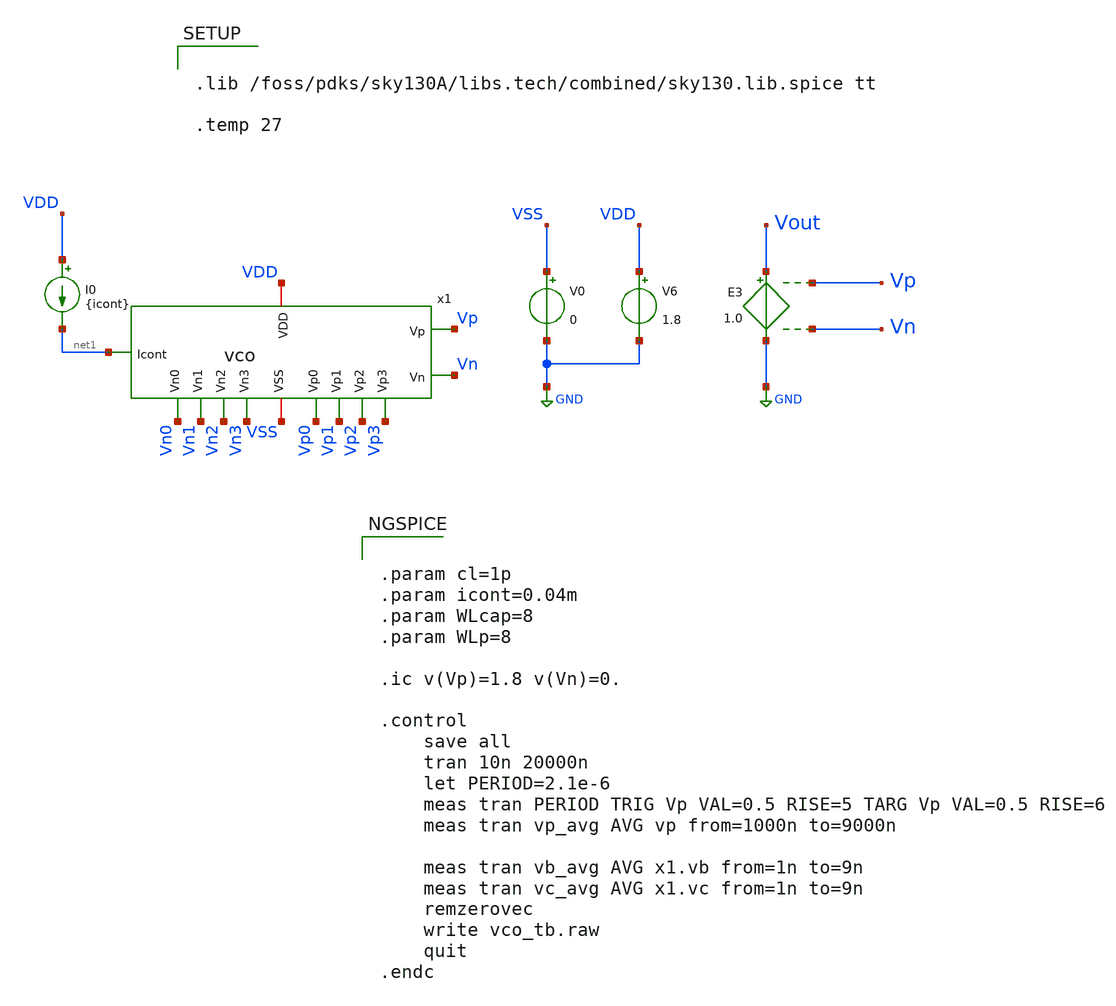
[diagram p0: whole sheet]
** sch_path: xschem/vco_tb.sch
**.subckt vco_tb
V0 VSS GND 0
V6 VDD GND 1.8
I0 VDD net1 {icont}
E3 Vout GND Vp Vn 1.0
x1 VDD VSS net1 Vp Vn Vp0 Vp1 Vp2 Vp3 Vn0 Vn1 Vn2 Vn3 vco
**** begin user architecture code


.param cl=1p
.param icont=0.04m
.param WLcap=8
.param WLp=8

.ic v(Vp)=1.8 v(Vn)=0.

.control
	save all
	tran 10n 20000n
	let PERIOD=2.1e-6
	meas tran PERIOD TRIG Vp VAL=0.5 RISE=5 TARG Vp VAL=0.5 RISE=6
	meas tran vp_avg AVG vp from=1000n to=9000n

	meas tran vb_avg AVG x1.vb from=1n to=9n
	meas tran vc_avg AVG x1.vc from=1n to=9n
	remzerovec
	write vco_tb.raw
	quit
.endc




.lib /foss/pdks/sky130A/libs.tech/combined/sky130.lib.spice tt

.temp 27


**** end user architecture code
**.ends

* expanding   symbol:  vco.sym # of pins=13
** sym_path: xschem/vco.sym
** sch_path: xschem/vco.sch
.subckt vco VDD VSS Icont Vp Vn Vp0 Vp1 Vp2 Vp3 Vn0 Vn1 Vn2 Vn3
*.iopin VDD
*.iopin VSS
*.ipin Icont
*.opin Vp
*.opin Vn
*.opin Vp0
*.opin Vp1
*.opin Vp2
*.opin Vp3
*.opin Vn0
*.opin Vn1
*.opin Vn2
*.opin Vn3
x1 VDD VSS Vp Vn Vb Vc net1 net2 vco_stage
x2 VDD VSS net1 net2 Vb Vc net3 net4 vco_stage
x3 VDD VSS net3 net4 Vb Vc Vpin1 Vnin1 vco_stage
x4 VDD VSS Vpin1 Vnin1 Vb Vc Vn Vp vco_stage
x5 VDD VSS Icont Vb Vc vco_bias
x6 VDD VSS net1 Vp0 vco_buffer
x7 VDD VSS net3 Vp1 vco_buffer
x8 VDD VSS Vpin1 Vp2 vco_buffer
x9 VDD VSS Vn Vp3 vco_buffer
x10 VDD VSS net2 Vn0 vco_buffer
x11 VDD VSS net4 Vn1 vco_buffer
x12 VDD VSS Vnin1 Vn2 vco_buffer
x13 VDD VSS Vp Vn3 vco_buffer
.ends


* expanding   symbol:  vco_stage.sym # of pins=8
** sym_path: xschem/vco_stage.sym
** sch_path: xschem/vco_stage.sch
.subckt vco_stage VDD VSS Vp Vn Vb Vc Vpout Vnout
*.iopin VDD
*.iopin VSS
*.ipin Vp
*.ipin Vn
*.ipin Vb
*.ipin Vc
*.opin Vpout
*.opin Vnout
XM5 Vds_m5 Vc VSS VSS sky130_fd_pr__nfet_01v8 L={L} W={W} nf=2 ad='int((nf+1)/2) * W/nf * 0.29' as='int((nf+2)/2) * W/nf * 0.29'
+ pd='2*int((nf+1)/2) * (W/nf + 0.29)' ps='2*int((nf+2)/2) * (W/nf + 0.29)' nrd='0.29 / W' nrs='0.29 / W'
+ sa=0 sb=0 sd=0 mult=1 m=1
x1 VDD VSS Vp Vb Vnout Vpout Vds_m5 vco_stage_half
x2 VDD VSS Vn Vb Vpout Vnout Vds_m5 vco_stage_half
.ends


* expanding   symbol:  vco_bias.sym # of pins=5
** sym_path: xschem/vco_bias.sym
** sch_path: xschem/vco_bias.sch
.subckt vco_bias VDD VSS Icont Vb Vc
*.iopin VDD
*.iopin VSS
*.ipin Icont
*.opin Vb
*.opin Vc
XM1 Icont Icont VSS VSS sky130_fd_pr__nfet_01v8 L=0.15 W=2 nf=1 ad='int((nf+1)/2) * W/nf * 0.29' as='int((nf+2)/2) * W/nf * 0.29'
+ pd='2*int((nf+1)/2) * (W/nf + 0.29)' ps='2*int((nf+2)/2) * (W/nf + 0.29)' nrd='0.29 / W' nrs='0.29 / W'
+ sa=0 sb=0 sd=0 mult=1 m=1
XM2 Vb Icont VSS VSS sky130_fd_pr__nfet_01v8 L=0.15 W=1 nf=1 ad='int((nf+1)/2) * W/nf * 0.29' as='int((nf+2)/2) * W/nf * 0.29'
+ pd='2*int((nf+1)/2) * (W/nf + 0.29)' ps='2*int((nf+2)/2) * (W/nf + 0.29)' nrd='0.29 / W' nrs='0.29 / W'
+ sa=0 sb=0 sd=0 mult=1 m=1
XM3 VDD Vb Vb VDD sky130_fd_pr__nfet_01v8 L=0.15 W=2 nf=1 ad='int((nf+1)/2) * W/nf * 0.29' as='int((nf+2)/2) * W/nf * 0.29'
+ pd='2*int((nf+1)/2) * (W/nf + 0.29)' ps='2*int((nf+2)/2) * (W/nf + 0.29)' nrd='0.29 / W' nrs='0.29 / W'
+ sa=0 sb=0 sd=0 mult=1 m=1
V1 Vc Icont 0
.ends


* expanding   symbol:  vco_buffer.sym # of pins=4
** sym_path: xschem/vco_buffer.sym
** sch_path: xschem/vco_buffer.sch
.subckt vco_buffer VDD VSS Vin Vout
*.iopin VDD
*.iopin VSS
*.ipin Vin
*.opin Vout
x1 VDD Vin net1 VSS vco_inverter
x2 VDD net1 Vout VSS vco_inverter
.ends


* expanding   symbol:  vco_stage_half.sym # of pins=7
** sym_path: xschem/vco_stage_half.sym
** sch_path: xschem/vco_stage_half.sch
.subckt vco_stage_half VDD VSS Vin Vb Vd Vout Vs
*.iopin VDD
*.iopin VSS
*.ipin Vin
*.ipin Vb
*.ipin Vd
*.opin Vout
*.opin Vs
XM8 VSS Vout VSS VSS sky130_fd_pr__nfet_01v8 L={WLcap} W={WLcap} nf=1 ad='int((nf+1)/2) * W/nf * 0.29'
+ as='int((nf+2)/2) * W/nf * 0.29' pd='2*int((nf+1)/2) * (W/nf + 0.29)' ps='2*int((nf+2)/2) * (W/nf + 0.29)'
+ nrd='0.29 / W' nrs='0.29 / W' sa=0 sb=0 sd=0 mult=1 m=1
XM7 Vout Vd VDD VDD sky130_fd_pr__pfet_01v8 L={L} W={W} nf=2 ad='int((nf+1)/2) * W/nf * 0.29' as='int((nf+2)/2) * W/nf * 0.29'
+ pd='2*int((nf+1)/2) * (W/nf + 0.29)' ps='2*int((nf+2)/2) * (W/nf + 0.29)' nrd='0.29 / W' nrs='0.29 / W'
+ sa=0 sb=0 sd=0 mult=1 m=1
XM3 Vout Vb VDD VDD sky130_fd_pr__pfet_01v8 L={L} W={W} nf=2 ad='int((nf+1)/2) * W/nf * 0.29' as='int((nf+2)/2) * W/nf * 0.29'
+ pd='2*int((nf+1)/2) * (W/nf + 0.29)' ps='2*int((nf+2)/2) * (W/nf + 0.29)' nrd='0.29 / W' nrs='0.29 / W'
+ sa=0 sb=0 sd=0 mult=1 m=1
XM1 Vout Vin Vs VSS sky130_fd_pr__nfet_01v8 L={L} W={W} nf=2 ad='int((nf+1)/2) * W/nf * 0.29' as='int((nf+2)/2) * W/nf * 0.29'
+ pd='2*int((nf+1)/2) * (W/nf + 0.29)' ps='2*int((nf+2)/2) * (W/nf + 0.29)' nrd='0.29 / W' nrs='0.29 / W'
+ sa=0 sb=0 sd=0 mult=1 m=1
.ends


* expanding   symbol:  vco_inverter.sym # of pins=4
** sym_path: xschem/vco_inverter.sym
** sch_path: xschem/vco_inverter.sch
.subckt vco_inverter VDD Vin Vout VSS
*.iopin VDD
*.iopin VSS
*.ipin Vin
*.opin Vout
XM1 Vout Vin VSS VSS sky130_fd_pr__nfet_01v8 L=0.15 W=1 nf=1 ad='int((nf+1)/2) * W/nf * 0.29' as='int((nf+2)/2) * W/nf * 0.29'
+ pd='2*int((nf+1)/2) * (W/nf + 0.29)' ps='2*int((nf+2)/2) * (W/nf + 0.29)' nrd='0.29 / W' nrs='0.29 / W'
+ sa=0 sb=0 sd=0 mult=1 m=1
XM2 Vout Vin VDD VDD sky130_fd_pr__pfet_01v8 L=0.15 W=1 nf=1 ad='int((nf+1)/2) * W/nf * 0.29' as='int((nf+2)/2) * W/nf * 0.29'
+ pd='2*int((nf+1)/2) * (W/nf + 0.29)' ps='2*int((nf+2)/2) * (W/nf + 0.29)' nrd='0.29 / W' nrs='0.29 / W'
+ sa=0 sb=0 sd=0 mult=1 m=1
.ends

.GLOBAL GND
.end
